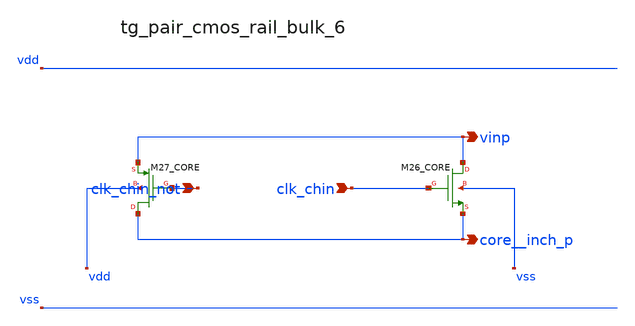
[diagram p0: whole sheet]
** sch_path: analog-db/raw/ia_006_fan_chopper_cmfb/hier/blocks/tg_pair_cmos_rail_bulk_6.sch
**.subckt tg_pair_cmos_rail_bulk_6 clk_chin_not clk_chin vinp core__inch_p
*.ipin clk_chin_not
*.ipin clk_chin
*.opin vinp
*.opin core__inch_p
XM26_CORE vinp clk_chin core__inch_p vss sg13_lv_nmos w=x_dut_xm26_core_w l=x_dut_xm26_core_l ng=1
+ m=x_dut_xm26_core_m
XM27_CORE core__inch_p clk_chin_not vinp vdd sg13_lv_pmos w=x_dut_xm27_core_w l=x_dut_xm27_core_l
+ ng=1 m=x_dut_xm27_core_m
**.ends
.end
